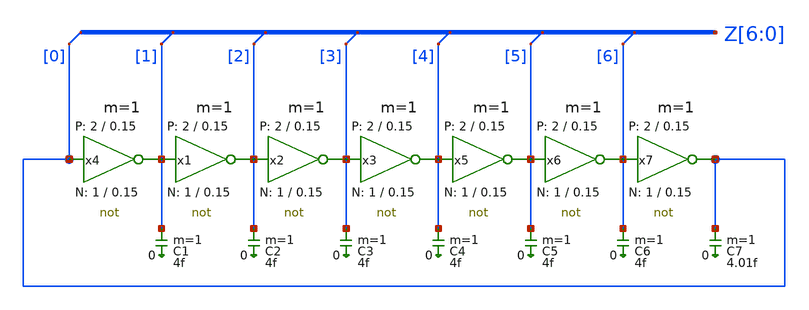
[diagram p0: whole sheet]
** sch_path: xschem/ring_test.sch
* StefanSchippers/xschem_sky130/sky130_tests/not.sch:
* Copyright 2021 Stefan Frederik Schippers
* Licensed under the Apache License, Version 2.0 (the "License");
**.subckt ring_test
C1 Z[1] 0 4f m=1
C2 Z[2] 0 4f m=1
C3 Z[3] 0 4f m=1
C4 Z[4] 0 4f m=1
C5 Z[5] 0 4f m=1
C6 Z[6] 0 4f m=1
C7 Z[0] 0 4.01f m=1
x4 Z[1] Z[0] VCC VSS not W_N=1 L_N=0.15 W_P=2 L_P=0.15 m=1
x1 Z[2] Z[1] VCC VSS not W_N=1 L_N=0.15 W_P=2 L_P=0.15 m=1
x2 Z[3] Z[2] VCC VSS not W_N=1 L_N=0.15 W_P=2 L_P=0.15 m=1
x3 Z[4] Z[3] VCC VSS not W_N=1 L_N=0.15 W_P=2 L_P=0.15 m=1
x5 Z[5] Z[4] VCC VSS not W_N=1 L_N=0.15 W_P=2 L_P=0.15 m=1
x6 Z[6] Z[5] VCC VSS not W_N=1 L_N=0.15 W_P=2 L_P=0.15 m=1
x7 Z[0] Z[6] VCC VSS not W_N=1 L_N=0.15 W_P=2 L_P=0.15 m=1
* tap: Z[6:0] --> Z[0]
* tap: Z[6:0] --> Z[1]
* tap: Z[6:0] --> Z[2]
* tap: Z[6:0] --> Z[3]
* tap: Z[6:0] --> Z[4]
* tap: Z[6:0] --> Z[5]
* tap: Z[6:0] --> Z[6]
**.ends

* expanding   symbol:  sky130_tests/not.sym # of pins=2
** sym_path: sky130_tests/not.sym
** sch_path: sky130_tests/not.sch
.subckt not y a VCCPIN VSSPIN     W_N=1 L_N=0.15 W_P=2 L_P=0.15
*.opin y
*.ipin a
XM1 DN a VSSPIN VSSPIN sky130_fd_pr__nfet_01v8 L=L_N W=W_N nf=1 ad='int((1 + 1)/2) * W_N / 1 * 0.29'
+ as='int((1 + 2)/2) * W_N / 1 * 0.29' pd='2*int((1 + 1)/2) * (W_N / 1 + 0.29)' ps='2*int((1 + 2)/2) * (W_N / 1 + 0.29)'
+ nrd='0.29 / W_N ' nrs='0.29 / W_N ' sa=0 sb=0 sd=0 mult=1 m=1
XM2 DP a VCCPIN VCCPIN sky130_fd_pr__pfet_01v8 L=L_P W=W_P nf=1 ad='int((nf+1)/2) * W/nf * 0.29' as='int((nf+2)/2) * W/nf * 0.29'
+ pd='2*int((nf+1)/2) * (W/nf + 0.29)' ps='2*int((nf+2)/2) * (W/nf + 0.29)' nrd='0.29 / W' nrs='0.29 / W'
+ sa=0 sb=0 sd=0 mult=1 m=1
Vmeas DP y 0
.save i(vmeas)
Vmeas1 y DN 0
.save i(vmeas1)
.save v(dp)
.save v(dn)
.ends

.end
